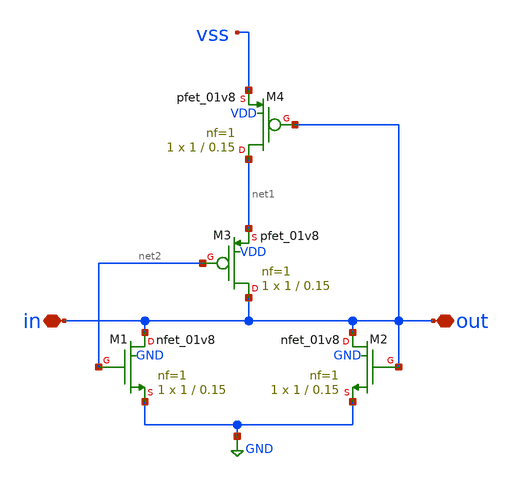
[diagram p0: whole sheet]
** sch_path: sch/nor.sch
**.subckt nor out in
*.iopin out
*.iopin in
XM1 out net2 GND GND sky130_fd_pr__nfet_01v8 L=0.15 W=1 nf=1 ad='int((nf+1)/2) * W/nf * 0.29' as='int((nf+2)/2) * W/nf * 0.29'
+ pd='2*int((nf+1)/2) * (W/nf + 0.29)' ps='2*int((nf+2)/2) * (W/nf + 0.29)' nrd='0.29 / W' nrs='0.29 / W'
+ sa=0 sb=0 sd=0 mult=1 m=1
XM2 out out GND GND sky130_fd_pr__nfet_01v8 L=0.15 W=1 nf=1 ad='int((nf+1)/2) * W/nf * 0.29' as='int((nf+2)/2) * W/nf * 0.29'
+ pd='2*int((nf+1)/2) * (W/nf + 0.29)' ps='2*int((nf+2)/2) * (W/nf + 0.29)' nrd='0.29 / W' nrs='0.29 / W'
+ sa=0 sb=0 sd=0 mult=1 m=1
XM3 out net2 net1 VDD sky130_fd_pr__pfet_01v8 L=0.15 W=1 nf=1 ad='int((nf+1)/2) * W/nf * 0.29' as='int((nf+2)/2) * W/nf * 0.29'
+ pd='2*int((nf+1)/2) * (W/nf + 0.29)' ps='2*int((nf+2)/2) * (W/nf + 0.29)' nrd='0.29 / W' nrs='0.29 / W'
+ sa=0 sb=0 sd=0 mult=1 m=1
XM4 net1 out vss VDD sky130_fd_pr__pfet_01v8 L=0.15 W=1 nf=1 ad='int((nf+1)/2) * W/nf * 0.29' as='int((nf+2)/2) * W/nf * 0.29'
+ pd='2*int((nf+1)/2) * (W/nf + 0.29)' ps='2*int((nf+2)/2) * (W/nf + 0.29)' nrd='0.29 / W' nrs='0.29 / W'
+ sa=0 sb=0 sd=0 mult=1 m=1
**.ends
.GLOBAL GND
.end
